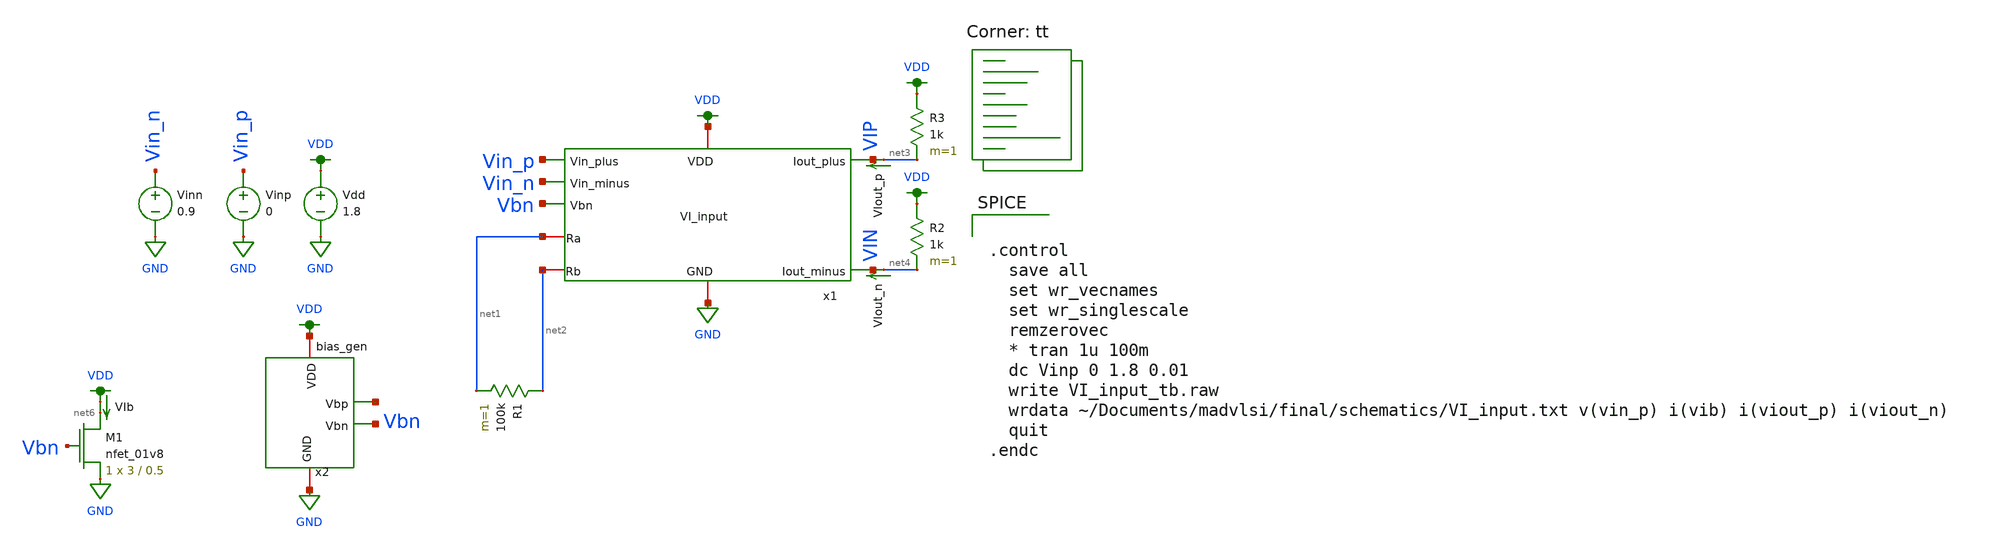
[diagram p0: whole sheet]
** sch_path: final/schematics/VI_input_tb.sch
**.subckt VI_input_tb
x1 VDD VIP VIN Vin_p Vin_n Vbn GND net1 net2 VI_input
Vdd VDD GND 1.8
x2 VDD net5 Vbn GND bias_gen
Vinp Vin_p GND 0
Vinn Vin_n GND 0.9
VIout_p net3 VIP 0
.save i(viout_p)
VIout_n net4 VIN 0
.save i(viout_n)
XM1 net6 Vbn GND GND sky130_fd_pr__nfet_01v8 L=0.5 W=3 nf=1 ad='int((nf+1)/2) * W/nf * 0.29' as='int((nf+2)/2) * W/nf * 0.29'
+ pd='2*int((nf+1)/2) * (W/nf + 0.29)' ps='2*int((nf+2)/2) * (W/nf + 0.29)' nrd='0.29 / W' nrs='0.29 / W'
+ sa=0 sb=0 sd=0 mult=1 m=1
VIb VDD net6 0
.save i(vib)
R2 VDD net4 1k m=1
R3 VDD net3 1k m=1
R1 net2 net1 100k m=1
**** begin user architecture code


.control
  save all
  set wr_vecnames
  set wr_singlescale
  remzerovec
  * tran 1u 100m
  dc Vinp 0 1.8 0.01
  write VI_input_tb.raw
  wrdata ~/Documents/madvlsi/final/schematics/VI_input.txt v(vin_p) i(vib) i(viout_p) i(viout_n)
  quit
.endc


.lib $::SKYWATER_MODELS/sky130.lib.spice tt
**** end user architecture code
**.ends

* expanding   symbol:  VI_input.sym # of pins=9
** sym_path: final/schematics/VI_input.sym
** sch_path: final/schematics/VI_input.sch
.subckt VI_input VDD Iout_plus Iout_minus Vin_plus Vin_minus Vbn GND Ra Rb
*.opin Iout_plus
*.opin Iout_minus
*.iopin VDD
*.ipin Vin_plus
*.ipin Vin_minus
*.ipin Vbn
*.iopin GND
*.iopin Ra
*.iopin Rb
X2 OPAMPN VDD GND Vin_minus Rb Vbn opamp
XM4 Rb Vbn GND GND sky130_fd_pr__nfet_01v8 L={len} W={wid} nf=1 ad='int((nf+1)/2) * W/nf * 0.29' as='int((nf+2)/2) * W/nf * 0.29'
+ pd='2*int((nf+1)/2) * (W/nf + 0.29)' ps='2*int((nf+2)/2) * (W/nf + 0.29)' nrd='0.29 / W' nrs='0.29 / W'
+ sa=0 sb=0 sd=0 mult=1 m=1
X1 OPAMPP VDD GND Vin_plus Ra Vbn opamp
XM3 Ra Vbn GND GND sky130_fd_pr__nfet_01v8 L={len} W={wid} nf=1 ad='int((nf+1)/2) * W/nf * 0.29' as='int((nf+2)/2) * W/nf * 0.29'
+ pd='2*int((nf+1)/2) * (W/nf + 0.29)' ps='2*int((nf+2)/2) * (W/nf + 0.29)' nrd='0.29 / W' nrs='0.29 / W'
+ sa=0 sb=0 sd=0 mult=1 m=1
**** begin user architecture code


.param wid=3 len=0.5


**** end user architecture code
XM1 Iout_plus OPAMPP Ra GND sky130_fd_pr__nfet_01v8 L={len} W={wid} nf=1 ad='int((nf+1)/2) * W/nf * 0.29'
+ as='int((nf+2)/2) * W/nf * 0.29' pd='2*int((nf+1)/2) * (W/nf + 0.29)' ps='2*int((nf+2)/2) * (W/nf + 0.29)'
+ nrd='0.29 / W' nrs='0.29 / W' sa=0 sb=0 sd=0 mult=1 m=1
XM2 Iout_minus OPAMPN Rb GND sky130_fd_pr__nfet_01v8 L={len} W={wid} nf=1 ad='int((nf+1)/2) * W/nf * 0.29'
+ as='int((nf+2)/2) * W/nf * 0.29' pd='2*int((nf+1)/2) * (W/nf + 0.29)' ps='2*int((nf+2)/2) * (W/nf + 0.29)'
+ nrd='0.29 / W' nrs='0.29 / W' sa=0 sb=0 sd=0 mult=1 m=1
.ends


* expanding   symbol:  /home/dt/Documents/madvlsi/final/schematics/bias_gen/bias_gen.sym # of pins=4
** sym_path: final/schematics/bias_gen/bias_gen.sym
** sch_path: final/schematics/bias_gen/bias_gen.sch
.subckt bias_gen VDD Vbp Vbn GND
*.iopin VDD
*.opin Vbp
*.iopin GND
*.opin Vbn
**** begin user architecture code

.param len=0.5 wid=3

**** end user architecture code
XM10 net3 net1 net1 GND sky130_fd_pr__nfet_01v8 L={len} W={wid} nf=1 ad='int((nf+1)/2) * W/nf * 0.29'
+ as='int((nf+2)/2) * W/nf * 0.29' pd='2*int((nf+1)/2) * (W/nf + 0.29)' ps='2*int((nf+2)/2) * (W/nf + 0.29)'
+ nrd='0.29 / W' nrs='0.29 / W' sa=0 sb=0 sd=0 mult=10 m=10
XM11 Vbn Vbn GND GND sky130_fd_pr__nfet_01v8 L={len} W={wid} nf=1 ad='int((nf+1)/2) * W/nf * 0.29' as='int((nf+2)/2) * W/nf * 0.29'
+ pd='2*int((nf+1)/2) * (W/nf + 0.29)' ps='2*int((nf+2)/2) * (W/nf + 0.29)' nrd='0.29 / W' nrs='0.29 / W'
+ sa=0 sb=0 sd=0 mult=1 m=1
XM12 GND Vbp GND GND sky130_fd_pr__nfet_01v8 L=10 W=10 nf=1 ad='int((nf+1)/2) * W/nf * 0.29' as='int((nf+2)/2) * W/nf * 0.29'
+ pd='2*int((nf+1)/2) * (W/nf + 0.29)' ps='2*int((nf+2)/2) * (W/nf + 0.29)' nrd='0.29 / W' nrs='0.29 / W'
+ sa=0 sb=0 sd=0 mult=1 m=1
XM13 VDD Vbp net1 VDD sky130_fd_pr__pfet_01v8 L={len} W={wid} nf=1 ad='int((nf+1)/2) * W/nf * 0.29' as='int((nf+2)/2) * W/nf * 0.29'
+ pd='2*int((nf+1)/2) * (W/nf + 0.29)' ps='2*int((nf+2)/2) * (W/nf + 0.29)' nrd='0.29 / W' nrs='0.29 / W'
+ sa=0 sb=0 sd=0 mult=1 m=1
XM14 GND Vbn Vbp GND sky130_fd_pr__nfet_01v8 L={len} W={wid} nf=1 ad='int((nf+1)/2) * W/nf * 0.29' as='int((nf+2)/2) * W/nf * 0.29'
+ pd='2*int((nf+1)/2) * (W/nf + 0.29)' ps='2*int((nf+2)/2) * (W/nf + 0.29)' nrd='0.29 / W' nrs='0.29 / W'
+ sa=0 sb=0 sd=0 mult=1 m=1
XM15 net2 net1 GND GND sky130_fd_pr__nfet_01v8 L={len} W={wid} nf=1 ad='int((nf+1)/2) * W/nf * 0.29'
+ as='int((nf+2)/2) * W/nf * 0.29' pd='2*int((nf+1)/2) * (W/nf + 0.29)' ps='2*int((nf+2)/2) * (W/nf + 0.29)'
+ nrd='0.29 / W' nrs='0.29 / W' sa=0 sb=0 sd=0 mult=1 m=1
XM16 VDD net2 net2 VDD sky130_fd_pr__pfet_01v8 L={len} W={wid} nf=1 ad='int((nf+1)/2) * W/nf * 0.29'
+ as='int((nf+2)/2) * W/nf * 0.29' pd='2*int((nf+1)/2) * (W/nf + 0.29)' ps='2*int((nf+2)/2) * (W/nf + 0.29)'
+ nrd='0.29 / W' nrs='0.29 / W' sa=0 sb=0 sd=0 mult=1 m=1
XM17 Vbp net2 VDD VDD sky130_fd_pr__pfet_01v8 L={len} W={wid} nf=1 ad='int((nf+1)/2) * W/nf * 0.29' as='int((nf+2)/2) * W/nf * 0.29'
+ pd='2*int((nf+1)/2) * (W/nf + 0.29)' ps='2*int((nf+2)/2) * (W/nf + 0.29)' nrd='0.29 / W' nrs='0.29 / W'
+ sa=0 sb=0 sd=0 mult=1 m=1
XM18 Vbn Vbp VDD VDD sky130_fd_pr__pfet_01v8 L={len} W={wid} nf=1 ad='int((nf+1)/2) * W/nf * 0.29' as='int((nf+2)/2) * W/nf * 0.29'
+ pd='2*int((nf+1)/2) * (W/nf + 0.29)' ps='2*int((nf+2)/2) * (W/nf + 0.29)' nrd='0.29 / W' nrs='0.29 / W'
+ sa=0 sb=0 sd=0 mult=1 m=1
XR2 GND net3 GND sky130_fd_pr__res_high_po_0p35 L=9 mult=1 m=1
.ends


* expanding   symbol:  opamp.sym # of pins=6
** sym_path: final/schematics/opamp.sym
** sch_path: final/schematics/opamp.sch
.subckt opamp Vout VDD GND Vplus Vminus Vbn
*.iopin VDD
*.iopin GND
*.ipin Vplus
*.ipin Vminus
*.opin Vout
*.ipin Vbn
XM3 net2 Vbn GND GND sky130_fd_pr__nfet_01v8 L={len} W={wid} nf=1 ad='int((nf+1)/2) * W/nf * 0.29' as='int((nf+2)/2) * W/nf * 0.29'
+ pd='2*int((nf+1)/2) * (W/nf + 0.29)' ps='2*int((nf+2)/2) * (W/nf + 0.29)' nrd='0.29 / W' nrs='0.29 / W'
+ sa=0 sb=0 sd=0 mult=1 m=1
XM4 net1 net1 VDD VDD sky130_fd_pr__pfet_01v8 L={len} W={wid} nf=1 ad='int((nf+1)/2) * W/nf * 0.29' as='int((nf+2)/2) * W/nf * 0.29'
+ pd='2*int((nf+1)/2) * (W/nf + 0.29)' ps='2*int((nf+2)/2) * (W/nf + 0.29)' nrd='0.29 / W' nrs='0.29 / W'
+ sa=0 sb=0 sd=0 mult=1 m=1
XM5 Vout net1 VDD VDD sky130_fd_pr__pfet_01v8 L={len} W={wid} nf=1 ad='int((nf+1)/2) * W/nf * 0.29' as='int((nf+2)/2) * W/nf * 0.29'
+ pd='2*int((nf+1)/2) * (W/nf + 0.29)' ps='2*int((nf+2)/2) * (W/nf + 0.29)' nrd='0.29 / W' nrs='0.29 / W'
+ sa=0 sb=0 sd=0 mult=1 m=1
XM1 net1 Vplus net2 GND sky130_fd_pr__nfet_01v8 L={len} W={wid} nf=1 ad='int((nf+1)/2) * W/nf * 0.29'
+ as='int((nf+2)/2) * W/nf * 0.29' pd='2*int((nf+1)/2) * (W/nf + 0.29)' ps='2*int((nf+2)/2) * (W/nf + 0.29)'
+ nrd='0.29 / W' nrs='0.29 / W' sa=0 sb=0 sd=0 mult=1 m=1
XM2 Vout Vminus net2 GND sky130_fd_pr__nfet_01v8 L={len} W={wid} nf=1 ad='int((nf+1)/2) * W/nf * 0.29'
+ as='int((nf+2)/2) * W/nf * 0.29' pd='2*int((nf+1)/2) * (W/nf + 0.29)' ps='2*int((nf+2)/2) * (W/nf + 0.29)'
+ nrd='0.29 / W' nrs='0.29 / W' sa=0 sb=0 sd=0 mult=1 m=1
**** begin user architecture code


.param wid=3 len=0.5


**** end user architecture code
.ends

.GLOBAL VDD
.GLOBAL GND
.end
